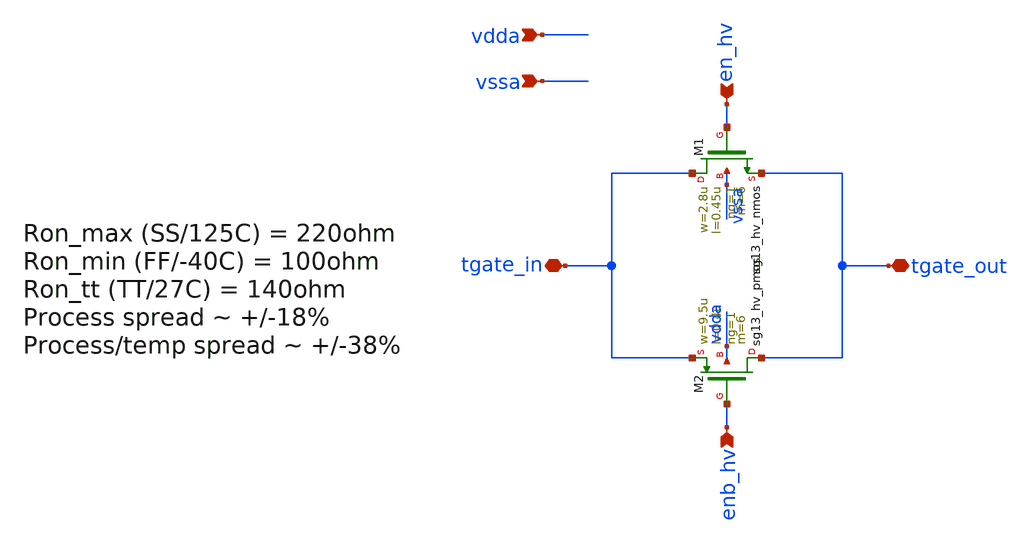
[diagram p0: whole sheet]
** sch_path: Schematics_Layout/sunrise_tgate/sunrise_tgate.sch
**.subckt sunrise_tgate vdda vssa tgate_in tgate_out en_hv enb_hv
*.ipin vdda
*.ipin vssa
*.iopin tgate_in
*.iopin tgate_out
*.ipin en_hv
*.ipin enb_hv
XM1 tgate_in en_hv tgate_out vssa sg13_hv_nmos w=2.8u l=0.45u ng=1 m=6 mm_ok=1
XM2 tgate_out enb_hv tgate_in vdda sg13_hv_pmos w=9.5u l=0.4u ng=1 m=6 mm_ok=1
**.ends
.end
